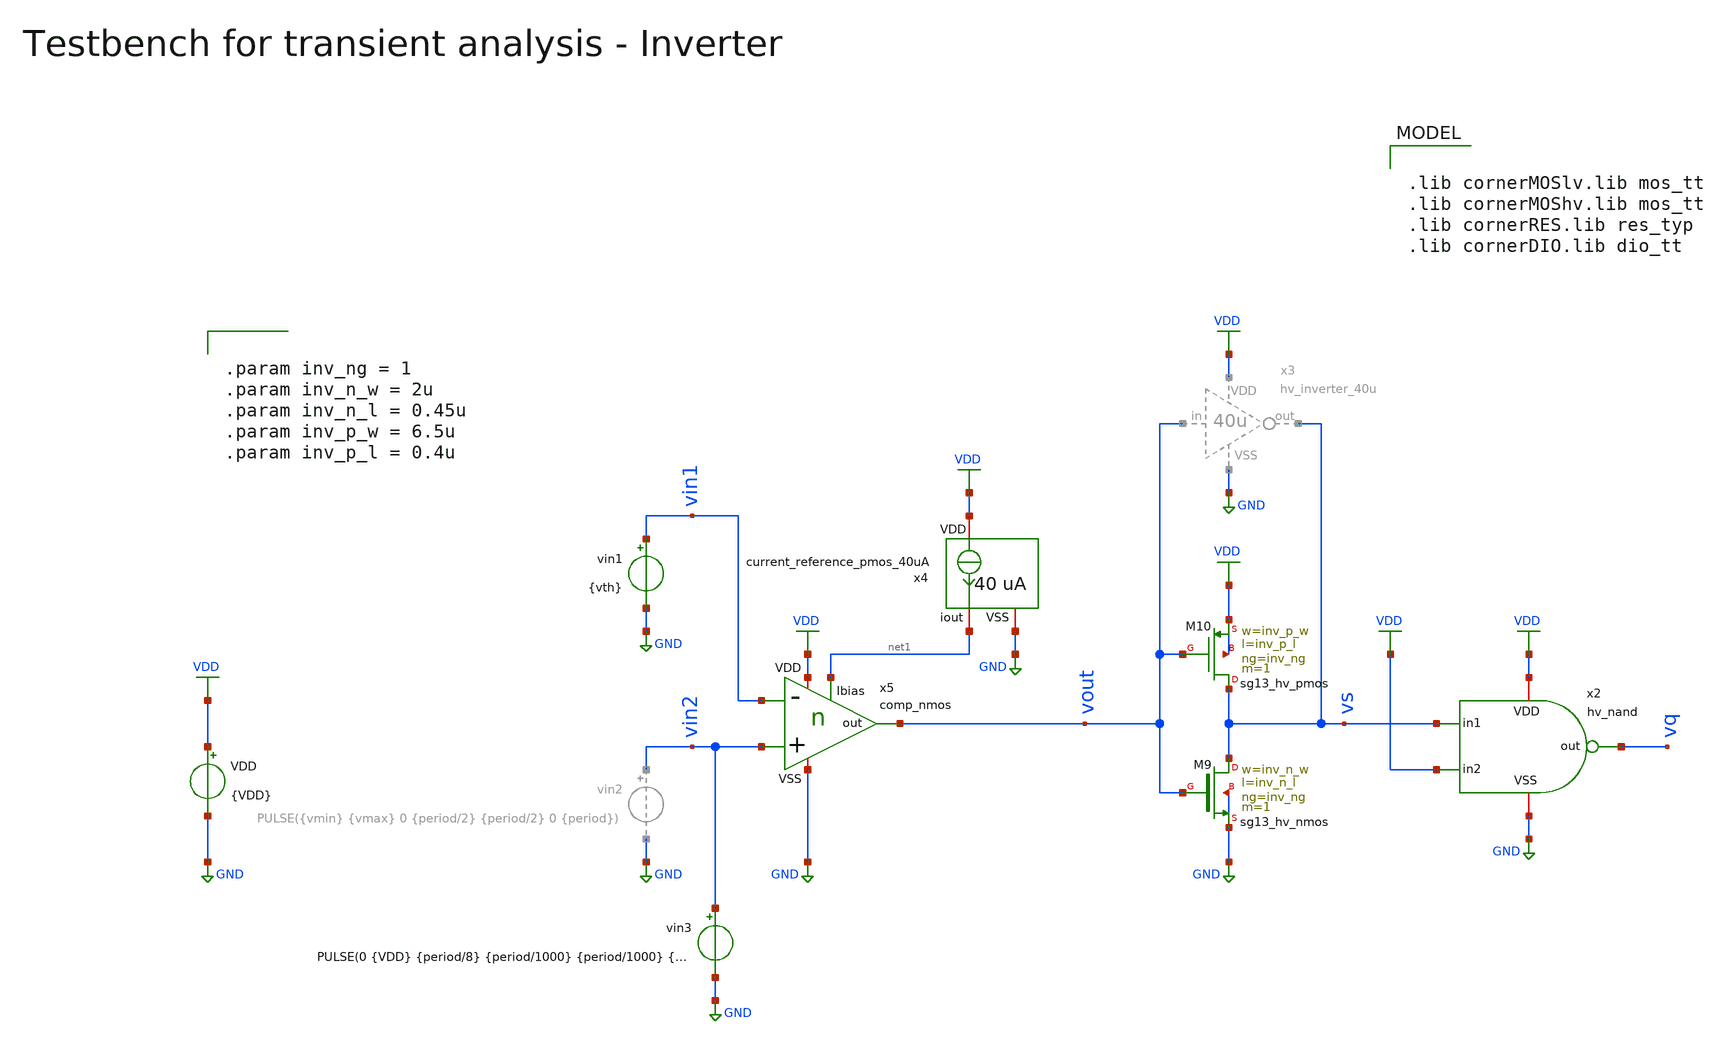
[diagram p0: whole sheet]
** sch_path: macros/heichips26_vcr/macros/switched_capacitor/testbenches/xschem/tb_comp_nmos_tran.sch
**.subckt tb_comp_nmos_tran
VDD VDD GND {VDD}
vin1 vin1 GND {vth}
x4 VDD net1 GND current_reference_pmos_40uA
x5 vout vin1 vin2 VDD net1 GND comp_nmos
XM9 vs vout GND GND sg13_hv_nmos w=inv_n_w l=inv_n_l ng=inv_ng m=1 mm_ok=1
XM10 vs vout VDD VDD sg13_hv_pmos w=inv_p_w l=inv_p_l ng=inv_ng m=1 mm_ok=1
x2 VDD vs vq VDD GND hv_nand
vin3 vin2 GND PULSE(0 {VDD} {period/8} {period/1000} {period/1000} {period/2} {period})
**** begin user architecture code


.param VDD=3.3
.csparam VDD=VDD
.param Vcm=VDD/2
.param temp=27
.param Cload=10p
.param Rload=1k

.param period = 5n
.csparam tstop  = {1*period}
.csparam tstep  = {period/100}

.param vth = 1.65
.param vpp = {period*2.65e+6}
.param vmax = {vth+vpp/2}
.param vmin = {vth-vpp/2}

.ic v(vq) = 0

.options savecurrents klu method=gear reltol=1e-4 abstol=1e-15 gmin=1e-15
.control

save all

* Operating Point Analysis
op
remzerovec
write @schname\.raw
set appendwrite

* Transient Analysis
tran {$&tstep} {$&tstop}
write @schname\.raw

* Plotting
plot vin1+4 vin2+4 vout vs vq+4
*plot vin1+4 50*(vin2-vin1)+4+vin1 vout vq+4
*plot vin1+4 vin2+4 vq+4 vout

* Write Data
unset appendwrite
set wr_vecnames
set wr_singlescale
*wrdata ../plot_simulations/data/@schname\.txt v(vin1) v(vin2) v(vout)

*quit
.endc



.lib cornerMOSlv.lib mos_tt
.lib cornerMOShv.lib mos_tt
.lib cornerRES.lib res_typ
.lib cornerDIO.lib dio_tt



.param inv_ng = 1
.param inv_n_w = 2u
.param inv_n_l = 0.45u
.param inv_p_w = 6.5u
.param inv_p_l = 0.4u


**** end user architecture code
**.ends

* expanding   symbol:  hv_inverter_40u.sym # of pins=4
** sym_path: macros/heichips26_vcr/macros/switched_capacitor/schematic/xschem/hv_inverter_40u.sym
** sch_path: macros/heichips26_vcr/macros/switched_capacitor/schematic/xschem/hv_inverter_40u.sch
.subckt hv_inverter_40u VDD in out VSS
*.ipin in
*.iopin VDD
*.iopin VSS
*.opin out
XM2 out in VSS VSS sg13_hv_nmos w={n_w} l={n_l} ng={ng} m=1 mm_ok=1
XM3 out in VDD VDD sg13_hv_pmos w={p_w} l={p_l} ng={ng} m=1 mm_ok=1
**** begin user architecture code


.param w   = 10u
.param ng  = 4
.param n_ng = ng
.param n_w = {3u*n_ng}
.param n_l = 0.45u
.param p_ng = ng
.param p_w = {10u*p_ng}
.param p_l = 0.4u


**** end user architecture code
.ends


* expanding   symbol:  current_reference_pmos_40uA.sym # of pins=3
** sym_path: macros/heichips26_vcr/macros/switched_capacitor/schematic/xschem/current_reference_pmos_40uA.sym
** sch_path: macros/heichips26_vcr/macros/switched_capacitor/schematic/xschem/current_reference_pmos_40uA.sch
.subckt current_reference_pmos_40uA VDD iout VSS
*.iopin VSS
*.iopin VDD
*.iopin iout
XM8 net1 net2 VSS VSS sg13_hv_nmos w=n_w l=n_l ng=1 m=1 mm_ok=1
XM6 net1 net1 VDD VDD sg13_hv_pmos w=p_w l=p_l ng=1 m=1 mm_ok=1
XM1 net2 net1 net3 VDD sg13_hv_pmos w=p_w l=p_l ng=1 m=1 mm_ok=1
XM3 net2 net2 VSS VSS sg13_hv_nmos w=n_w l=n_l ng=1 m=1 mm_ok=1
XR2 VDD net4 VSS rppd w=2e-6 l=21.6e-6 m=1 b=0 mm_ok=1
XR3 net4 net3 VSS rsil w=0.5e-6 l=282e-6 m=1 mm_ok=1
**** begin user architecture code


.param n_w = 6u
.param n_l = 5u
.param p_w = 10u
.param p_l = 2u


**** end user architecture code
XM2 net2 net1 net3 VDD sg13_hv_pmos w=p_w l=p_l ng=1 m=1 mm_ok=1
XM4 net2 net1 net3 VDD sg13_hv_pmos w=p_w l=p_l ng=1 m=1 mm_ok=1
XM5 net2 net1 net3 VDD sg13_hv_pmos w=p_w l=p_l ng=1 m=1 mm_ok=1
XM7 iout net1 VDD VDD sg13_hv_pmos w=p_w l=p_l ng=1 m=1 mm_ok=1
.ends


* expanding   symbol:  comp_nmos.sym # of pins=6
** sym_path: macros/heichips26_vcr/macros/switched_capacitor/schematic/xschem/comp_nmos.sym
** sch_path: macros/heichips26_vcr/macros/switched_capacitor/schematic/xschem/comp_nmos.sch
.subckt comp_nmos out - + VDD Ibias VSS
*.iopin VDD
*.iopin VSS
*.ipin -
*.ipin +
*.ipin Ibias
*.opin out
XM8 net2 + net3 VSS sg13_hv_nmos w=n_w l=n_l ng=1 m=1 mm_ok=1
XM6 net1 net1 VDD VDD sg13_hv_pmos w=p_w l=p_l ng=1 m=1 mm_ok=1
XM1 net2 net1 VDD VDD sg13_hv_pmos w=p_w l=p_l ng=1 m=1 mm_ok=1
XM3 net1 - net3 VSS sg13_hv_nmos w=n_w l=n_l ng=1 m=1 mm_ok=1
**** begin user architecture code


.param n_w = 1.2u
.param n_l = 1.5u
.param p_w = 2u
.param p_l = 0.4u


**** end user architecture code
XM2 out net2 VDD VDD sg13_hv_pmos w=p_w l=p_l ng=1 m=1 mm_ok=1
XM4 net3 Ibias VSS VSS sg13_hv_nmos w=2*n_w l=n_l ng=1 m=1 mm_ok=1
XM5 out Ibias VSS VSS sg13_hv_nmos w=2*n_w l=n_l ng=1 m=1 mm_ok=1
XM7 Ibias Ibias VSS VSS sg13_hv_nmos w=n_w l=n_l ng=1 m=1 mm_ok=1
.ends


* expanding   symbol:  hv_nand.sym # of pins=5
** sym_path: macros/heichips26_vcr/macros/switched_capacitor/schematic/xschem/hv_nand.sym
** sch_path: macros/heichips26_vcr/macros/switched_capacitor/schematic/xschem/hv_nand.sch
.subckt hv_nand VDD in1 out in2 VSS
*.ipin in1
*.iopin VDD
*.iopin VSS
*.opin out
*.ipin in2
**** begin user architecture code


.param w   = 10u
.param ng  = 4
.param n_ng = ng
.param n_w = {3u*n_ng}
.param n_l = 0.45u
.param p_ng = ng
.param p_w = {10u*p_ng}
.param p_l = 0.4u


**** end user architecture code
XM2 out in1 net1 VSS sg13_hv_nmos w={n_w} l={n_l} ng={ng} m=1 mm_ok=1
XM3 out in2 VDD VDD sg13_hv_pmos w={p_w} l={p_l} ng={ng} m=1 mm_ok=1
XM1 net1 in2 VSS VSS sg13_hv_nmos w={n_w} l={n_l} ng={ng} m=1 mm_ok=1
XM4 out in1 VDD VDD sg13_hv_pmos w={p_w} l={p_l} ng={ng} m=1 mm_ok=1
.ends

.GLOBAL GND
.GLOBAL VDD
.end
